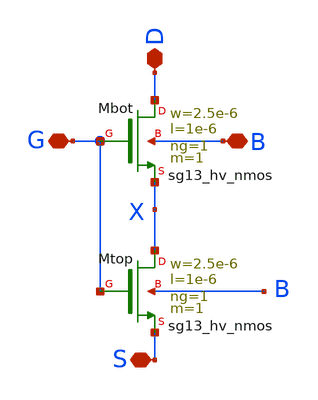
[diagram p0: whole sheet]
** sch_path: macros/comparator/schematic/xschem/n1_2.sch
**.subckt n1_2 G D S B
*.iopin G
*.iopin D
*.iopin S
*.iopin B
XMbot D G X B sg13_hv_nmos w=2.5e-6 l=1e-6 ng=1 m=1 mm_ok=1
XMtop X G S B sg13_hv_nmos w=2.5e-6 l=1e-6 ng=1 m=1 mm_ok=1
**.ends
.end
